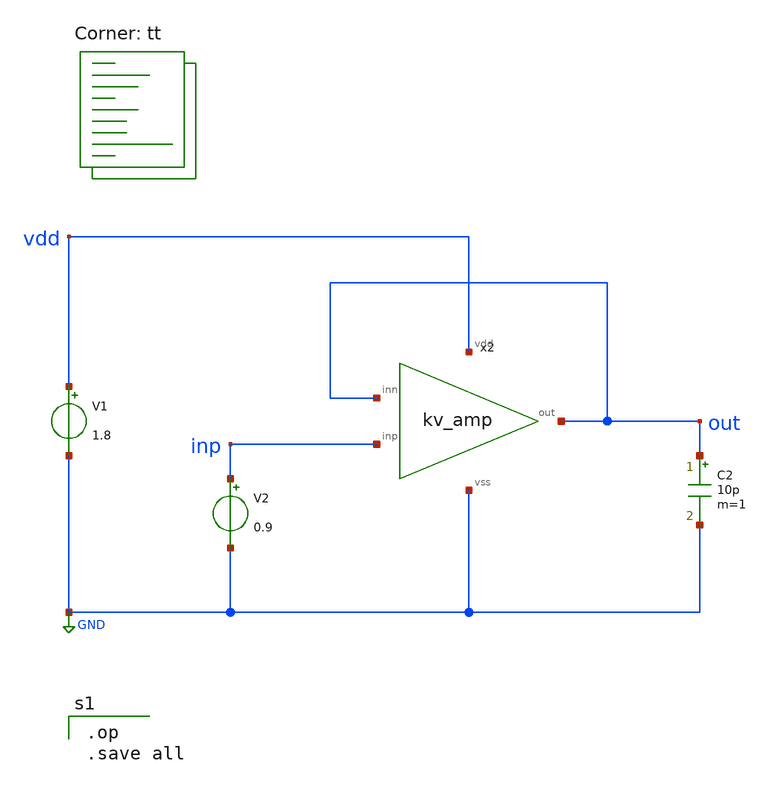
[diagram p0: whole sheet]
** sch_path: examples/demo_tapeout/xschem/tb_amp.sch
**.subckt tb_amp
V1 vdd GND 1.8
V2 inp GND 0.9
x2 vdd GND inp out out kv_amp
C2 out GND 10p m=1
**** begin user architecture code
.lib $::SKYWATER_MODELS/sky130.lib.spice tt

.op
.save all

**** end user architecture code
**.ends

* expanding   symbol:  kv_amp.sym # of pins=5
** sym_path: examples/demo_tapeout/xschem/kv_amp.sym
** sch_path: examples/demo_tapeout/xschem/kv_amp.sch
.subckt kv_amp vdd vss inp inn out
*.iopin vdd
*.iopin vss
*.iopin inp
*.iopin inn
*.iopin out
XM3 o1 o1 vdd vdd sky130_fd_pr__pfet_01v8 L=1 W=8 nf=1 ad='int((nf+1)/2) * W/nf * 0.29' as='int((nf+2)/2) * W/nf * 0.29'
+ pd='2*int((nf+1)/2) * (W/nf + 0.29)' ps='2*int((nf+2)/2) * (W/nf + 0.29)' nrd='0.29 / W' nrs='0.29 / W'
+ sa=0 sb=0 sd=0 mult=1 m=1
XM4 o2a o1 vdd vdd sky130_fd_pr__pfet_01v8 L=1 W=8 nf=1 ad='int((nf+1)/2) * W/nf * 0.29' as='int((nf+2)/2) * W/nf * 0.29'
+ pd='2*int((nf+1)/2) * (W/nf + 0.29)' ps='2*int((nf+2)/2) * (W/nf + 0.29)' nrd='0.29 / W' nrs='0.29 / W'
+ sa=0 sb=0 sd=0 mult=1 m=1
XM7 out o2a vdd vdd sky130_fd_pr__pfet_01v8 L=0.5 W=32 nf=1 ad='int((nf+1)/2) * W/nf * 0.29' as='int((nf+2)/2) * W/nf * 0.29'
+ pd='2*int((nf+1)/2) * (W/nf + 0.29)' ps='2*int((nf+2)/2) * (W/nf + 0.29)' nrd='0.29 / W' nrs='0.29 / W'
+ sa=0 sb=0 sd=0 mult=1 m=1
XM1 o1 inn tail vss sky130_fd_pr__nfet_01v8 L=1 W=8 nf=1 ad='int((1 + 1)/2) * 8 / 1 * 0.29' as='int((1 + 2)/2) * 8 / 1 * 0.29'
+ pd='2*int((1 + 1)/2) * (8 / 1 + 0.29)' ps='2*int((1 + 2)/2) * (8 / 1 + 0.29)' nrd='0.29 / 8 ' nrs='0.29 / 8 '
+ sa=0 sb=0 sd=0 mult=1 m=1
XM2 o2a inp tail vss sky130_fd_pr__nfet_01v8 L=1 W=8 nf=1 ad='int((1 + 1)/2) * 8 / 1 * 0.29' as='int((1 + 2)/2) * 8 / 1 * 0.29'
+ pd='2*int((1 + 1)/2) * (8 / 1 + 0.29)' ps='2*int((1 + 2)/2) * (8 / 1 + 0.29)' nrd='0.29 / 8 ' nrs='0.29 / 8 '
+ sa=0 sb=0 sd=0 mult=1 m=1
XM5 tail vb vss vss sky130_fd_pr__nfet_01v8 L=1 W=8 nf=1 ad='int((1 + 1)/2) * 8 / 1 * 0.29' as='int((1 + 2)/2) * 8 / 1 * 0.29'
+ pd='2*int((1 + 1)/2) * (8 / 1 + 0.29)' ps='2*int((1 + 2)/2) * (8 / 1 + 0.29)' nrd='0.29 / 8 ' nrs='0.29 / 8 '
+ sa=0 sb=0 sd=0 mult=1 m=1
XM6 vb vb vss vss sky130_fd_pr__nfet_01v8 L=1 W=4 nf=1 ad='int((1 + 1)/2) * 4 / 1 * 0.29' as='int((1 + 2)/2) * 4 / 1 * 0.29'
+ pd='2*int((1 + 1)/2) * (4 / 1 + 0.29)' ps='2*int((1 + 2)/2) * (4 / 1 + 0.29)' nrd='0.29 / 4 ' nrs='0.29 / 4 '
+ sa=0 sb=0 sd=0 mult=1 m=1
XM8 out vb vss vss sky130_fd_pr__nfet_01v8 L=1 W=16 nf=1 ad='int((1 + 1)/2) * 16 / 1 * 0.29' as='int((1 + 2)/2) * 16 / 1 * 0.29'
+ pd='2*int((1 + 1)/2) * (16 / 1 + 0.29)' ps='2*int((1 + 2)/2) * (16 / 1 + 0.29)' nrd='0.29 / 16 ' nrs='0.29 / 16 '
+ sa=0 sb=0 sd=0 mult=1 m=1
I1 vdd vb 20u
C1 o2a ncz 0.5p m=1
R1 ncz out 2k m=1
.ends

.GLOBAL GND
.end
